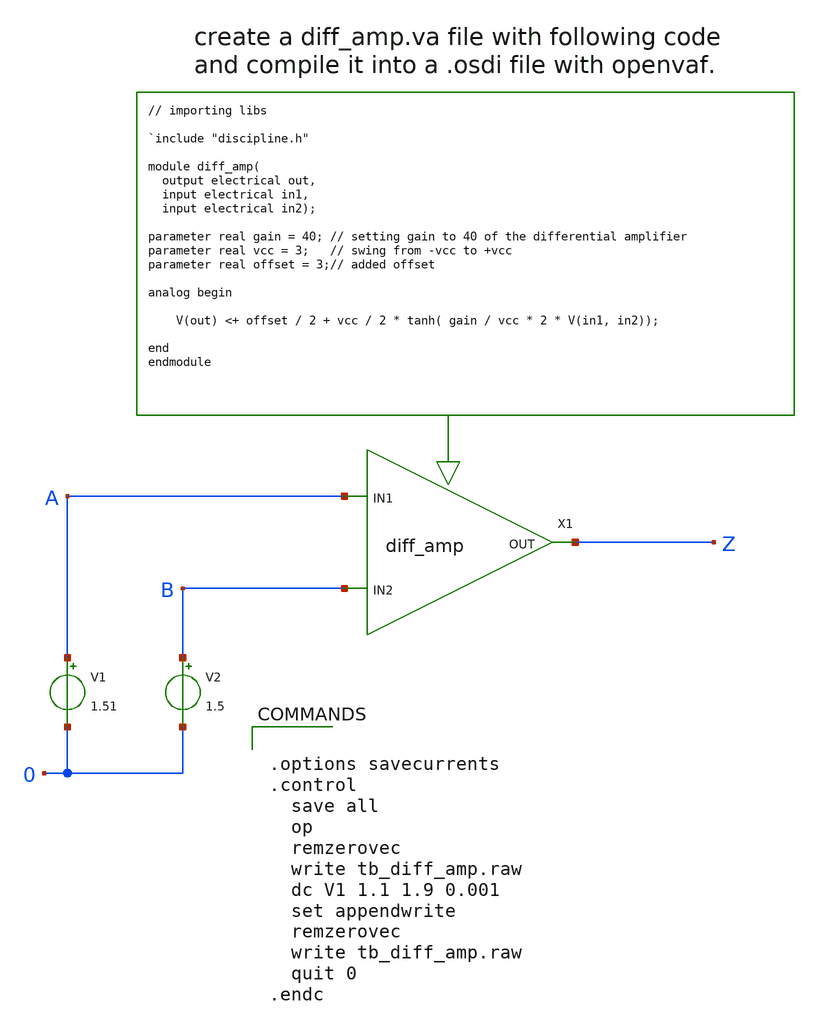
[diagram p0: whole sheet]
** sch_path: xschem_library/ngspice/tb_diff_amp.sch
* Copyright (C) 1998-2024 Stefan Frederik Schippers
* This program is free software; you can redistribute it and/or modify
* it under the terms of the GNU General Public License as published by
* the Free Software Foundation; either version 2 of the License, or
* (at your option) any later version.
* This program is distributed in the hope that it will be useful,
* but WITHOUT ANY WARRANTY; without even the implied warranty of
* MERCHANTABILITY or FITNESS FOR A PARTICULAR PURPOSE.  See the
* GNU General Public License for more details.
* You should have received a copy of the GNU General Public License
* along with this program; if not, write to the Free Software
**.subckt tb_diff_amp
X1 Z A B diff_amp_cell
V1 A 0 1.51
V2 B 0 1.5
**** begin user architecture code


.options savecurrents
.control
  save all
  op
  remzerovec
  write tb_diff_amp.raw
  dc V1 1.1 1.9 0.001
  set appendwrite
  remzerovec
  write tb_diff_amp.raw
  quit 0
.endc


**** end user architecture code
**.ends
**** begin user architecture code

.subckt diff_amp_cell OUT IN1 IN2
N1 out in1 in2 diff_amp_model
.ends diff_amp_cell

.model diff_amp_model diff_amp

.control
* following line specifies the location for the .osdi file so ngspice can use it.
pre_osdi $USER_CONF_DIR/xschem_library/diff_amp.osdi
.endc

**** end user architecture code
.end
